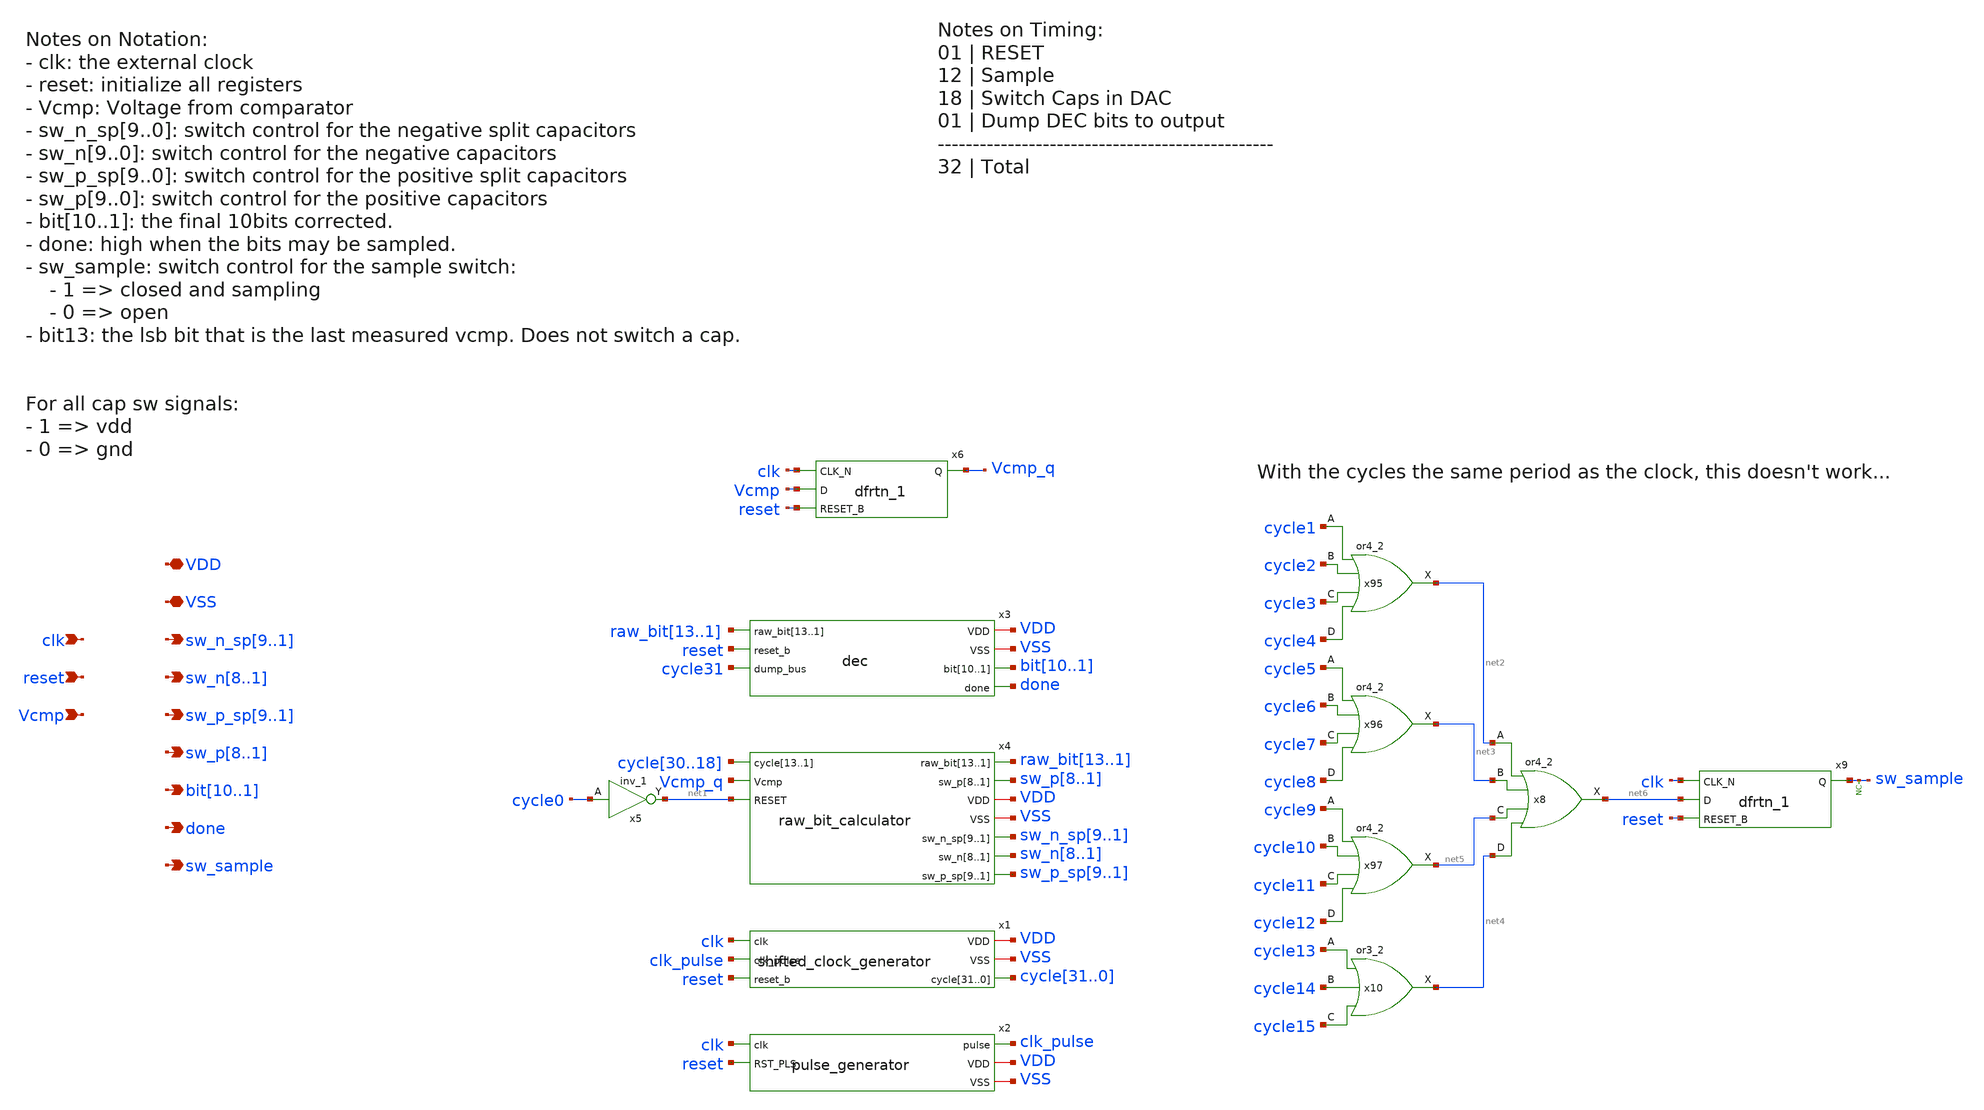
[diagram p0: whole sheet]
** sch_path: xschem/src/controller/controller.sch
**.subckt controller clk
*+ sw_n_sp9,sw_n_sp8,sw_n_sp7,sw_n_sp6,sw_n_sp5,sw_n_sp4,sw_n_sp3,sw_n_sp2,sw_n_sp1 VSS VDD reset Vcmp sw_n8,sw_n7,sw_n6,sw_n5,sw_n4,sw_n3,sw_n2,sw_n1
*+ sw_p_sp9,sw_p_sp8,sw_p_sp7,sw_p_sp6,sw_p_sp5,sw_p_sp4,sw_p_sp3,sw_p_sp2,sw_p_sp1 sw_p8,sw_p7,sw_p6,sw_p5,sw_p4,sw_p3,sw_p2,sw_p1 bit10,bit9,bit8,bit7,bit6,bit5,bit4,bit3,bit2,bit1
*+ done sw_sample
*.ipin clk
*.opin sw_n_sp9,sw_n_sp8,sw_n_sp7,sw_n_sp6,sw_n_sp5,sw_n_sp4,sw_n_sp3,sw_n_sp2,sw_n_sp1
*.iopin VSS
*.iopin VDD
*.ipin reset
*.ipin Vcmp
*.opin sw_n8,sw_n7,sw_n6,sw_n5,sw_n4,sw_n3,sw_n2,sw_n1
*.opin sw_p_sp9,sw_p_sp8,sw_p_sp7,sw_p_sp6,sw_p_sp5,sw_p_sp4,sw_p_sp3,sw_p_sp2,sw_p_sp1
*.opin sw_p8,sw_p7,sw_p6,sw_p5,sw_p4,sw_p3,sw_p2,sw_p1
*.opin bit10,bit9,bit8,bit7,bit6,bit5,bit4,bit3,bit2,bit1
*.opin done
*.opin sw_sample
x95 cycle1 cycle2 cycle3 cycle4 VSS VSS VDD VDD net2 sky130_fd_sc_hd__or4_2
x96 cycle5 cycle6 cycle7 cycle8 VSS VSS VDD VDD net3 sky130_fd_sc_hd__or4_2
x97 cycle9 cycle10 cycle11 cycle12 VSS VSS VDD VDD net5 sky130_fd_sc_hd__or4_2
* noconn sw_sample
x2 clk clk_pulse VDD VSS reset pulse_generator
x3 VDD raw_bit13 raw_bit12 raw_bit11 raw_bit10 raw_bit9 raw_bit8 raw_bit7 raw_bit6 raw_bit5 raw_bit4
+ raw_bit3 raw_bit2 raw_bit1 VSS reset bit10 bit9 bit8 bit7 bit6 bit5 bit4 bit3 bit2 bit1 done cycle31 dec
x4 raw_bit13 raw_bit12 raw_bit11 raw_bit10 raw_bit9 raw_bit8 raw_bit7 raw_bit6 raw_bit5 raw_bit4
+ raw_bit3 raw_bit2 raw_bit1 cycle30 cycle29 cycle28 cycle27 cycle26 cycle25 cycle24 cycle23 cycle22 cycle21
+ cycle20 cycle19 cycle18 sw_p8 sw_p7 sw_p6 sw_p5 sw_p4 sw_p3 sw_p2 sw_p1 Vcmp_q net1 VDD VSS sw_n_sp9
+ sw_n_sp8 sw_n_sp7 sw_n_sp6 sw_n_sp5 sw_n_sp4 sw_n_sp3 sw_n_sp2 sw_n_sp1 sw_n8 sw_n7 sw_n6 sw_n5 sw_n4 sw_n3
+ sw_n2 sw_n1 sw_p_sp9 sw_p_sp8 sw_p_sp7 sw_p_sp6 sw_p_sp5 sw_p_sp4 sw_p_sp3 sw_p_sp2 sw_p_sp1
+ raw_bit_calculator
x5 cycle0 VSS VSS VDD VDD net1 sky130_fd_sc_hd__inv_1
x1 clk VDD VSS clk_pulse reset cycle31 cycle30 cycle29 cycle28 cycle27 cycle26 cycle25 cycle24
+ cycle23 cycle22 cycle21 cycle20 cycle19 cycle18 cycle17 cycle16 cycle15 cycle14 cycle13 cycle12 cycle11
+ cycle10 cycle9 cycle8 cycle7 cycle6 cycle5 cycle4 cycle3 cycle2 cycle1 cycle0 shifted_clock_generator
x6 clk Vcmp reset VSS VSS VDD VDD Vcmp_q sky130_fd_sc_hd__dfrtn_1
x8 net2 net3 net5 net4 VSS VSS VDD VDD net6 sky130_fd_sc_hd__or4_2
x9 clk net6 reset VSS VSS VDD VDD sw_sample sky130_fd_sc_hd__dfrtn_1
x10 cycle13 cycle14 cycle15 VSS VSS VDD VDD net4 sky130_fd_sc_hd__or3_2
**.ends
.end
